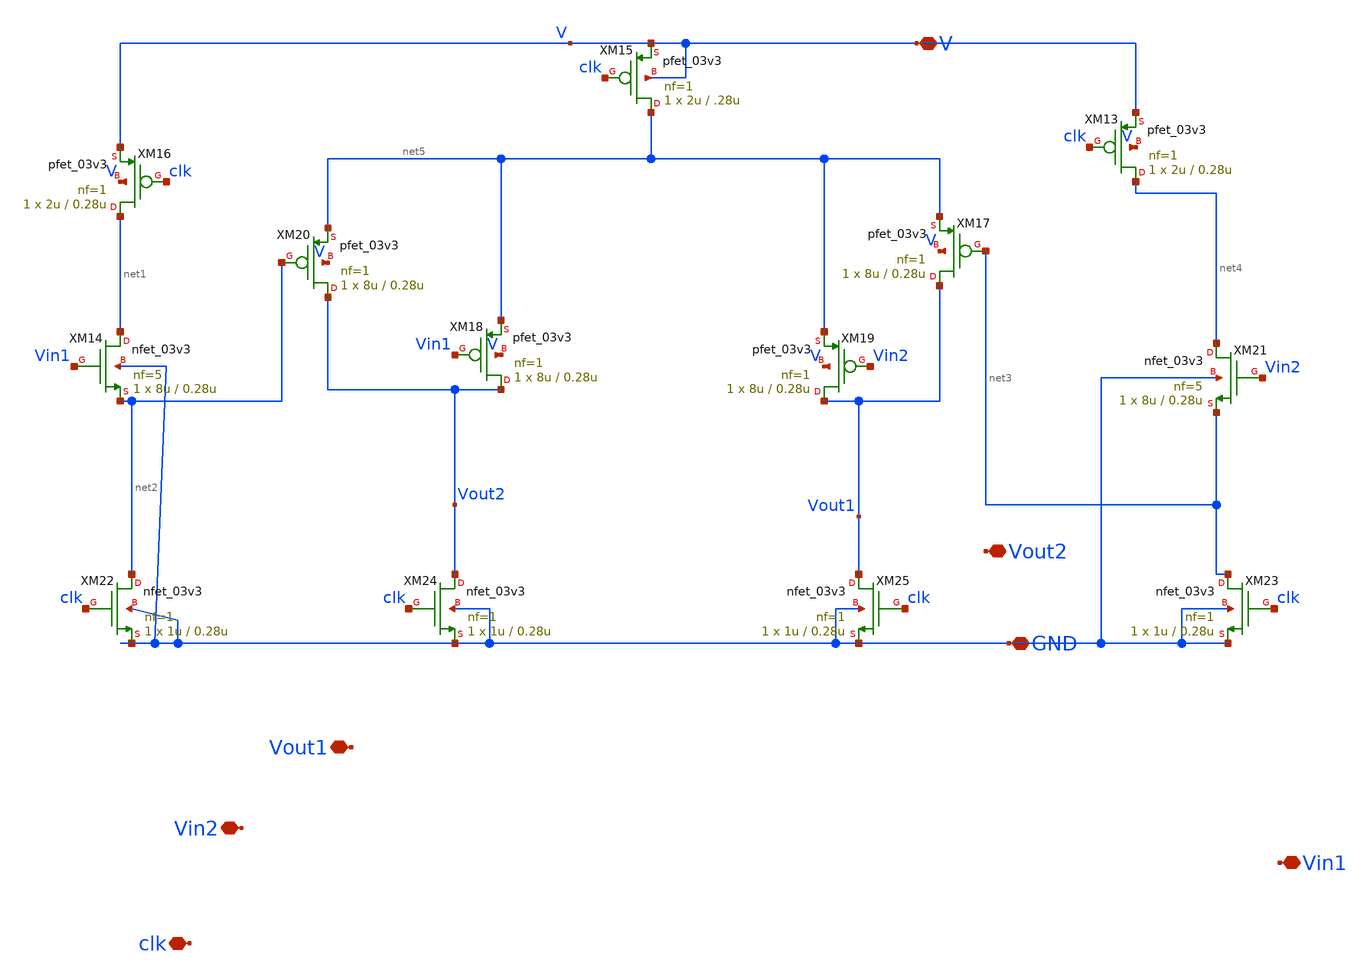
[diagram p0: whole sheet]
** sch_path: xschem/designs/preamp_2.sch
**.subckt preamp_2 GND Vout2 Vout1 clk Vin2 Vin1 V
*.iopin GND
*.iopin Vout2
*.iopin Vout1
*.iopin clk
*.iopin Vin2
*.iopin Vin1
*.iopin V
XM13 net4 clk V V pfet_03v3 L=0.28u W=2u nf=1 ad='int((nf+1)/2) * W/nf * 0.18u' as='int((nf+2)/2) * W/nf * 0.18u'
+ pd='2*int((nf+1)/2) * (W/nf + 0.18u)' ps='2*int((nf+2)/2) * (W/nf + 0.18u)' nrd='0.18u / W' nrs='0.18u / W'
+ sa=0 sb=0 sd=0 m=1
XM14 net1 Vin1 net2 GND nfet_03v3 L=0.28u W=8u nf=5 ad='int((nf+1)/2) * W/nf * 0.18u' as='int((nf+2)/2) * W/nf * 0.18u'
+ pd='2*int((nf+1)/2) * (W/nf + 0.18u)' ps='2*int((nf+2)/2) * (W/nf + 0.18u)' nrd='0.18u / W' nrs='0.18u / W'
+ sa=0 sb=0 sd=0 m=1
XM15 net5 clk V V pfet_03v3 L=.28u W=2u nf=1 ad='int((nf+1)/2) * W/nf * 0.18u' as='int((nf+2)/2) * W/nf * 0.18u'
+ pd='2*int((nf+1)/2) * (W/nf + 0.18u)' ps='2*int((nf+2)/2) * (W/nf + 0.18u)' nrd='0.18u / W' nrs='0.18u / W'
+ sa=0 sb=0 sd=0 m=1
XM16 net1 clk V V pfet_03v3 L=0.28u W=2u nf=1 ad='int((nf+1)/2) * W/nf * 0.18u' as='int((nf+2)/2) * W/nf * 0.18u'
+ pd='2*int((nf+1)/2) * (W/nf + 0.18u)' ps='2*int((nf+2)/2) * (W/nf + 0.18u)' nrd='0.18u / W' nrs='0.18u / W'
+ sa=0 sb=0 sd=0 m=1
XM17 Vout1 net3 net5 V pfet_03v3 L=0.28u W=8u nf=1 ad='int((nf+1)/2) * W/nf * 0.18u' as='int((nf+2)/2) * W/nf * 0.18u'
+ pd='2*int((nf+1)/2) * (W/nf + 0.18u)' ps='2*int((nf+2)/2) * (W/nf + 0.18u)' nrd='0.18u / W' nrs='0.18u / W'
+ sa=0 sb=0 sd=0 m=1
XM18 Vout2 Vin1 net5 V pfet_03v3 L=0.28u W=8u nf=1 ad='int((nf+1)/2) * W/nf * 0.18u' as='int((nf+2)/2) * W/nf * 0.18u'
+ pd='2*int((nf+1)/2) * (W/nf + 0.18u)' ps='2*int((nf+2)/2) * (W/nf + 0.18u)' nrd='0.18u / W' nrs='0.18u / W'
+ sa=0 sb=0 sd=0 m=1
XM19 Vout1 Vin2 net5 V pfet_03v3 L=0.28u W=8u nf=1 ad='int((nf+1)/2) * W/nf * 0.18u' as='int((nf+2)/2) * W/nf * 0.18u'
+ pd='2*int((nf+1)/2) * (W/nf + 0.18u)' ps='2*int((nf+2)/2) * (W/nf + 0.18u)' nrd='0.18u / W' nrs='0.18u / W'
+ sa=0 sb=0 sd=0 m=1
XM20 Vout2 net2 net5 V pfet_03v3 L=0.28u W=8u nf=1 ad='int((nf+1)/2) * W/nf * 0.18u' as='int((nf+2)/2) * W/nf * 0.18u'
+ pd='2*int((nf+1)/2) * (W/nf + 0.18u)' ps='2*int((nf+2)/2) * (W/nf + 0.18u)' nrd='0.18u / W' nrs='0.18u / W'
+ sa=0 sb=0 sd=0 m=1
XM21 net4 Vin2 net3 GND nfet_03v3 L=0.28u W=8u nf=5 ad='int((nf+1)/2) * W/nf * 0.18u' as='int((nf+2)/2) * W/nf * 0.18u'
+ pd='2*int((nf+1)/2) * (W/nf + 0.18u)' ps='2*int((nf+2)/2) * (W/nf + 0.18u)' nrd='0.18u / W' nrs='0.18u / W'
+ sa=0 sb=0 sd=0 m=1
XM22 net2 clk GND GND nfet_03v3 L=0.28u W=1u nf=1 ad='int((nf+1)/2) * W/nf * 0.18u' as='int((nf+2)/2) * W/nf * 0.18u'
+ pd='2*int((nf+1)/2) * (W/nf + 0.18u)' ps='2*int((nf+2)/2) * (W/nf + 0.18u)' nrd='0.18u / W' nrs='0.18u / W'
+ sa=0 sb=0 sd=0 m=1
XM23 net3 clk GND GND nfet_03v3 L=0.28u W=1u nf=1 ad='int((nf+1)/2) * W/nf * 0.18u' as='int((nf+2)/2) * W/nf * 0.18u'
+ pd='2*int((nf+1)/2) * (W/nf + 0.18u)' ps='2*int((nf+2)/2) * (W/nf + 0.18u)' nrd='0.18u / W' nrs='0.18u / W'
+ sa=0 sb=0 sd=0 m=1
XM24 Vout2 clk GND GND nfet_03v3 L=0.28u W=1u nf=1 ad='int((nf+1)/2) * W/nf * 0.18u' as='int((nf+2)/2) * W/nf * 0.18u'
+ pd='2*int((nf+1)/2) * (W/nf + 0.18u)' ps='2*int((nf+2)/2) * (W/nf + 0.18u)' nrd='0.18u / W' nrs='0.18u / W'
+ sa=0 sb=0 sd=0 m=1
XM25 Vout1 clk GND GND nfet_03v3 L=0.28u W=1u nf=1 ad='int((nf+1)/2) * W/nf * 0.18u' as='int((nf+2)/2) * W/nf * 0.18u'
+ pd='2*int((nf+1)/2) * (W/nf + 0.18u)' ps='2*int((nf+2)/2) * (W/nf + 0.18u)' nrd='0.18u / W' nrs='0.18u / W'
+ sa=0 sb=0 sd=0 m=1
**.ends
.end
